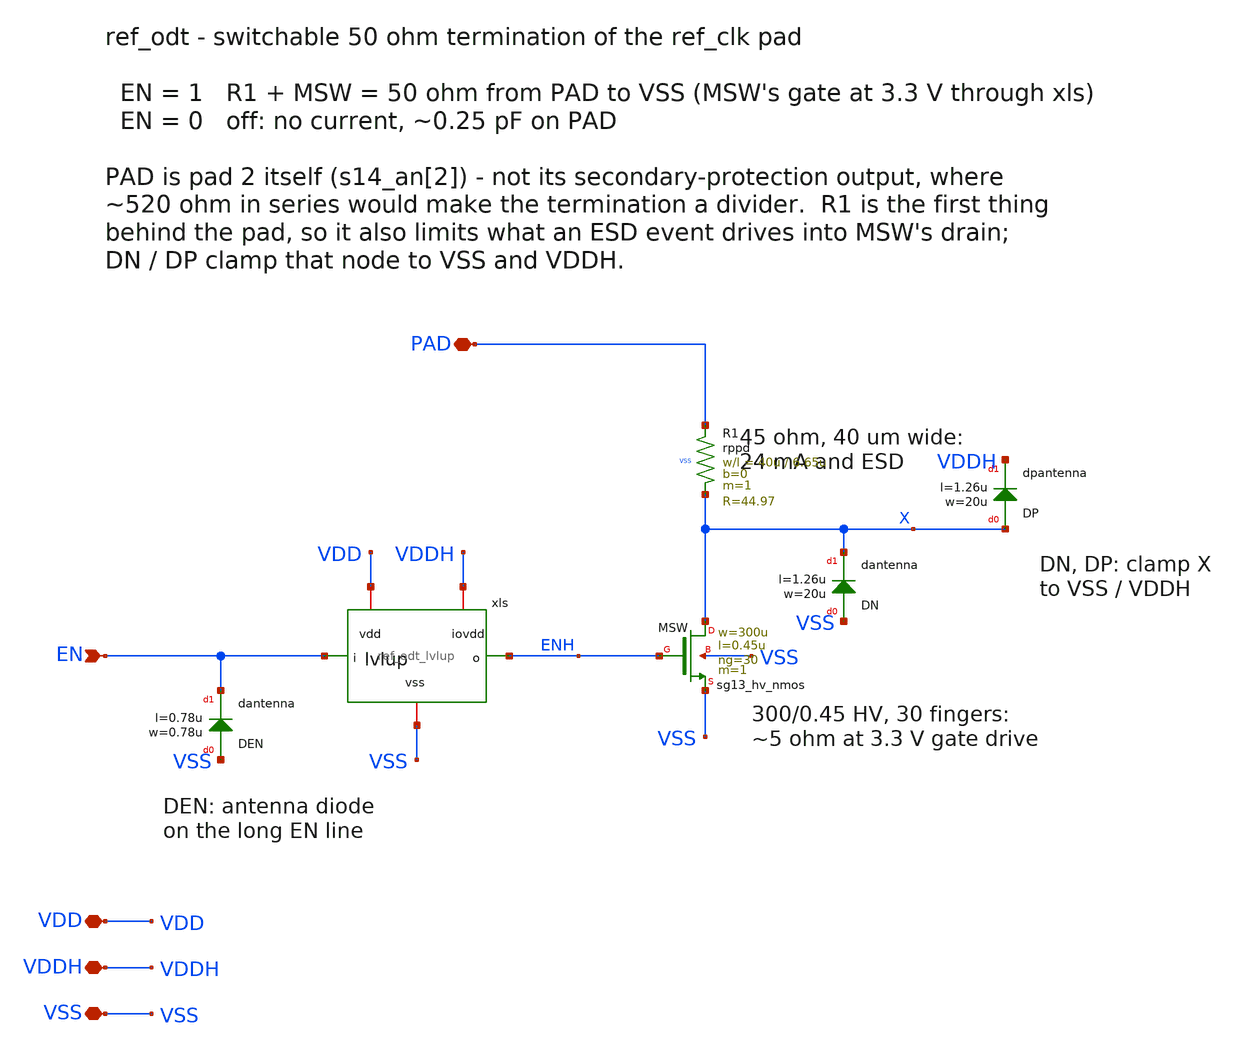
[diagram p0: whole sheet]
** sch_path: macros/ref_odt/schematic/xschem/ref_odt.sch
**.subckt ref_odt PAD EN VDD VDDH VSS
*.iopin PAD
*.ipin EN
*.iopin VDD
*.iopin VDDH
*.iopin VSS
XR1 PAD X VSS rppd w=40u l=6.65u m=1 b=0 mm_ok=1
XDN VSS X dantenna l=1.26u w=20u
XDP X VDDH dpantenna l=1.26u w=20u
XMSW X ENH VSS VSS sg13_hv_nmos w=300u l=0.45u ng=30 m=1 mm_ok=1
xls EN ENH VDD VDDH VSS ref_odt_lvlup
XDEN VSS EN dantenna l=0.78u w=0.78u
**.ends

* expanding   symbol:  ref_odt_lvlup.sym # of pins=5
** sym_path: macros/ref_odt/schematic/xschem/ref_odt_lvlup.sym
** sch_path: macros/ref_odt/schematic/xschem/ref_odt_lvlup.sch
.subckt ref_odt_lvlup i o vdd iovdd vss
*.ipin i
*.opin o
*.iopin vdd
*.iopin iovdd
*.iopin vss
XMP_I IN_N i vdd vdd sg13_lv_pmos w=4.75u l=0.13u ng=1 m=1 mm_ok=1
XMN_I IN_N i vss vss sg13_lv_nmos w=2.75u l=0.13u ng=1 m=1 mm_ok=1
XMP_LN LVLD_N LVLD iovdd iovdd sg13_hv_pmos w=0.3u l=0.45u ng=1 m=1 mm_ok=1
XMN_LN LVLD_N i vss vss sg13_hv_nmos w=1.9u l=0.45u ng=1 m=1 mm_ok=1
XMP_L LVLD LVLD_N iovdd iovdd sg13_hv_pmos w=0.3u l=0.45u ng=1 m=1 mm_ok=1
XMN_L LVLD IN_N vss vss sg13_hv_nmos w=1.9u l=0.45u ng=1 m=1 mm_ok=1
XMP_O o LVLD_N iovdd iovdd sg13_hv_pmos w=3.9u l=0.45u ng=1 m=1 mm_ok=1
XMN_O o LVLD_N vss vss sg13_hv_nmos w=1.9u l=0.45u ng=1 m=1 mm_ok=1
.ends

.end
